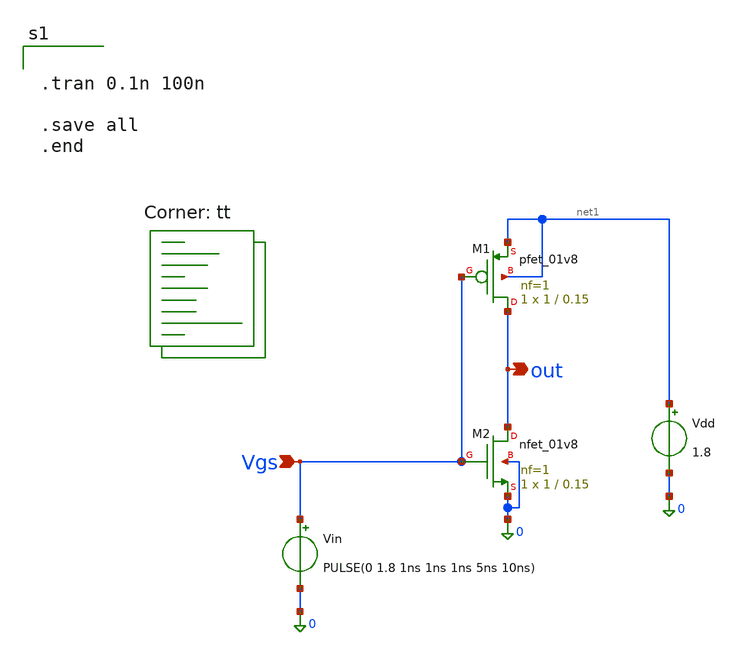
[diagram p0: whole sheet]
** sch_path: BGR_TOP_SKY130A/MOS_charec.sch
**.subckt MOS_charec Vgs out
*.ipin Vgs
*.opin out
XM2 out Vgs 0 0 sky130_fd_pr__nfet_01v8 L=0.15 W=1 nf=1 ad='int((1 + 1)/2) * 1 / 1 * 0.29' as='int((1 + 2)/2) * 1 / 1 * 0.29'
+ pd='2*int((1 + 1)/2) * (1 / 1 + 0.29)' ps='2*int((1 + 2)/2) * (1 / 1 + 0.29)' nrd='0.29 / 1 ' nrs='0.29 / 1 '
+ sa=0 sb=0 sd=0 mult=1 m=1
Vin Vgs 0 PULSE(0 1.8 1ns 1ns 1ns 5ns 10ns)
Vdd net1 0 1.8
XM1 out Vgs net1 net1 sky130_fd_pr__pfet_01v8 L=0.15 W=1 nf=1 ad='int((1 + 1)/2) * 1 / 1 * 0.29' as='int((1 + 2)/2) * 1 / 1 * 0.29'
+ pd='2*int((1 + 1)/2) * (1 / 1 + 0.29)' ps='2*int((1 + 2)/2) * (1 / 1 + 0.29)' nrd='0.29 / 1 ' nrs='0.29 / 1 '
+ sa=0 sb=0 sd=0 mult=1 m=1
**** begin user architecture code
.lib $::SKYWATER_MODELS/sky130.lib.spice tt


.tran 0.1n 100n

.save all
.end


**** end user architecture code
**.ends
.end
